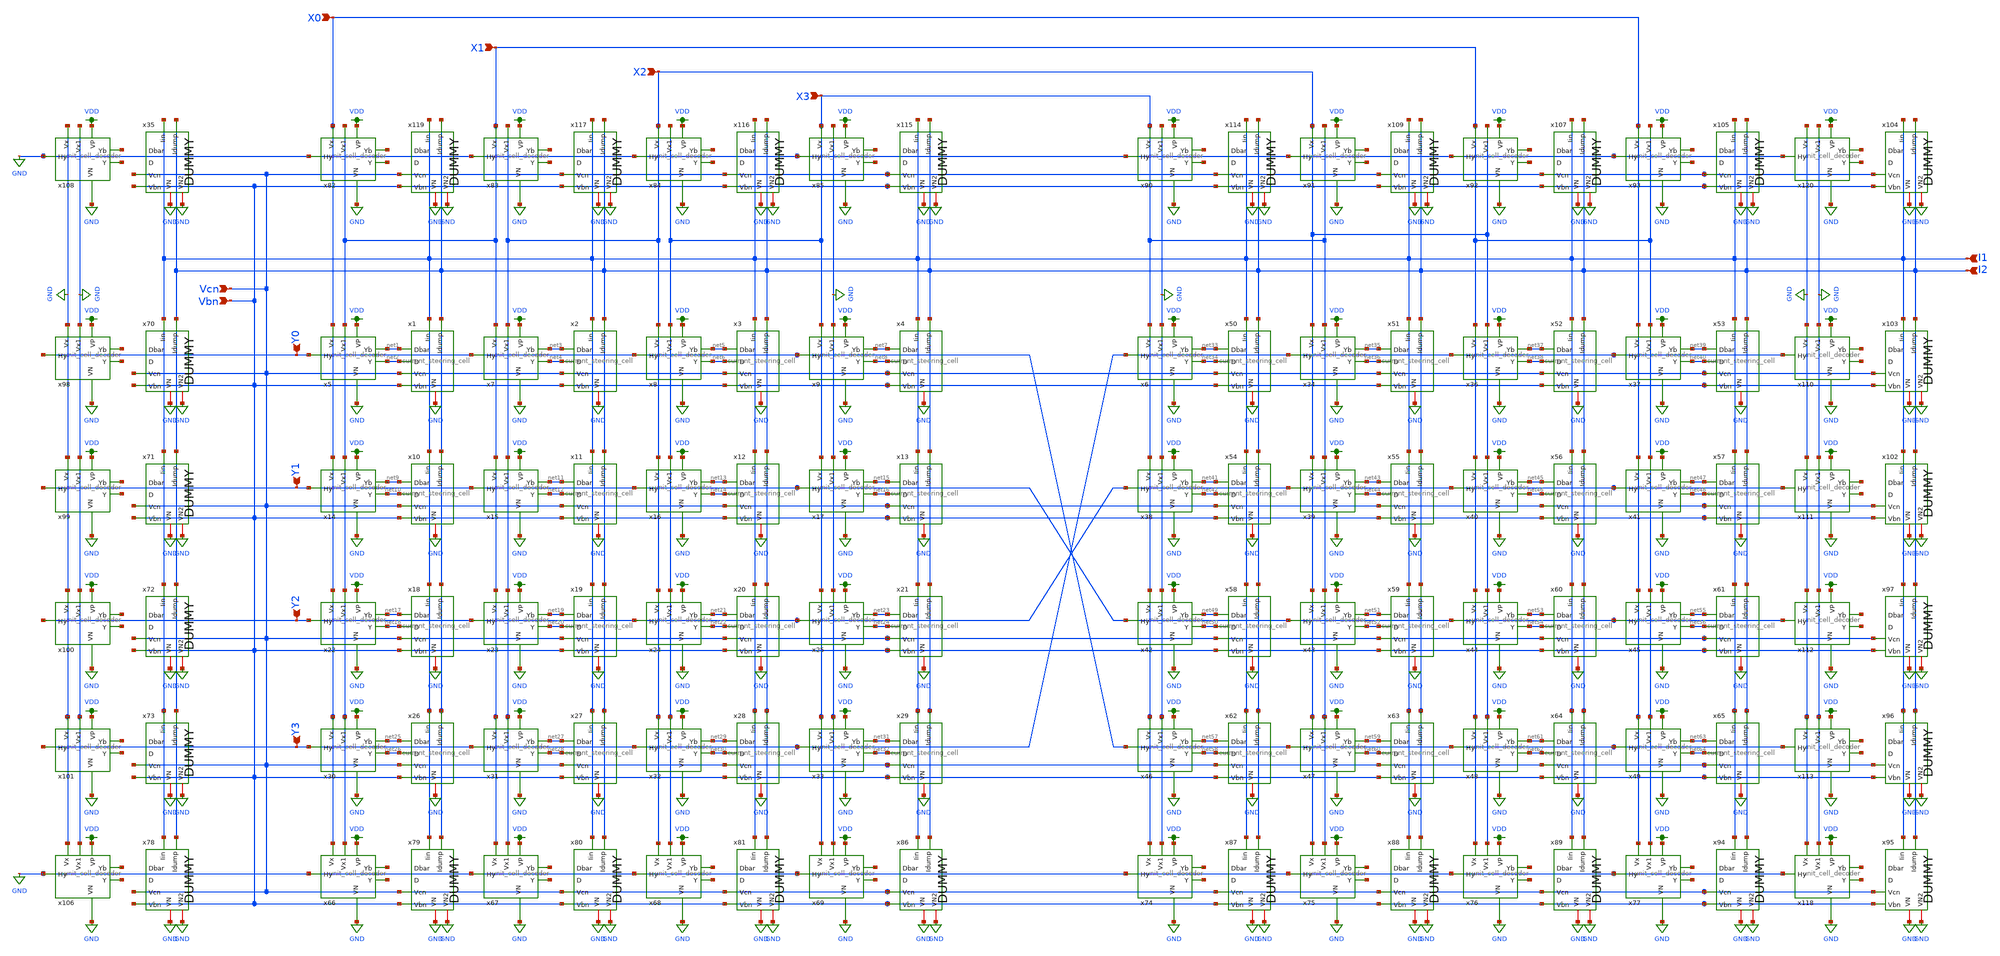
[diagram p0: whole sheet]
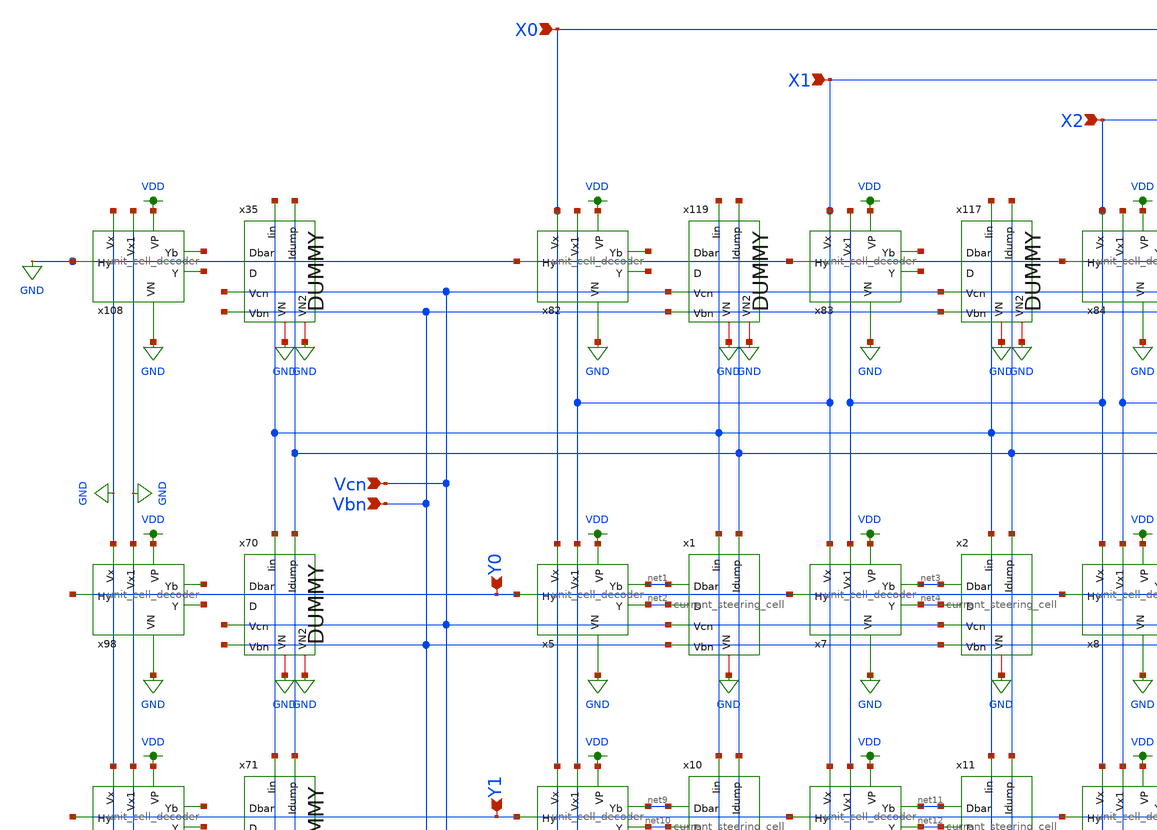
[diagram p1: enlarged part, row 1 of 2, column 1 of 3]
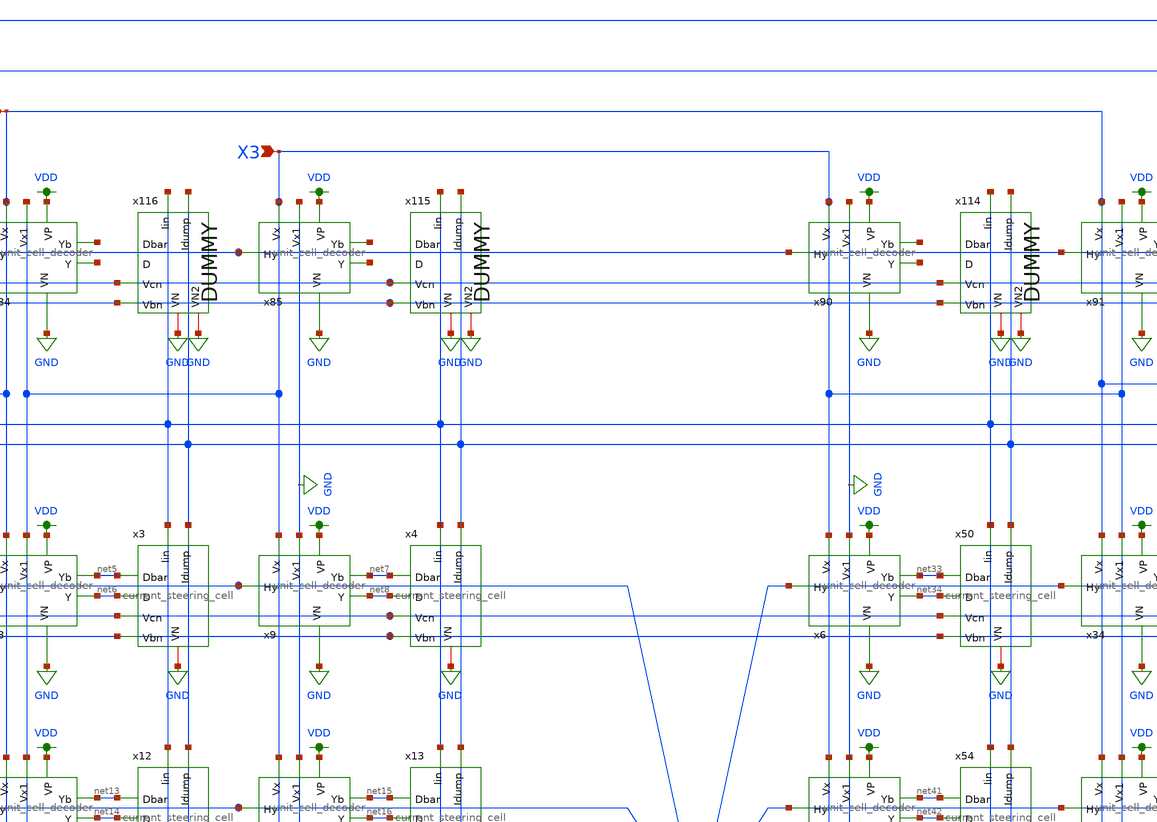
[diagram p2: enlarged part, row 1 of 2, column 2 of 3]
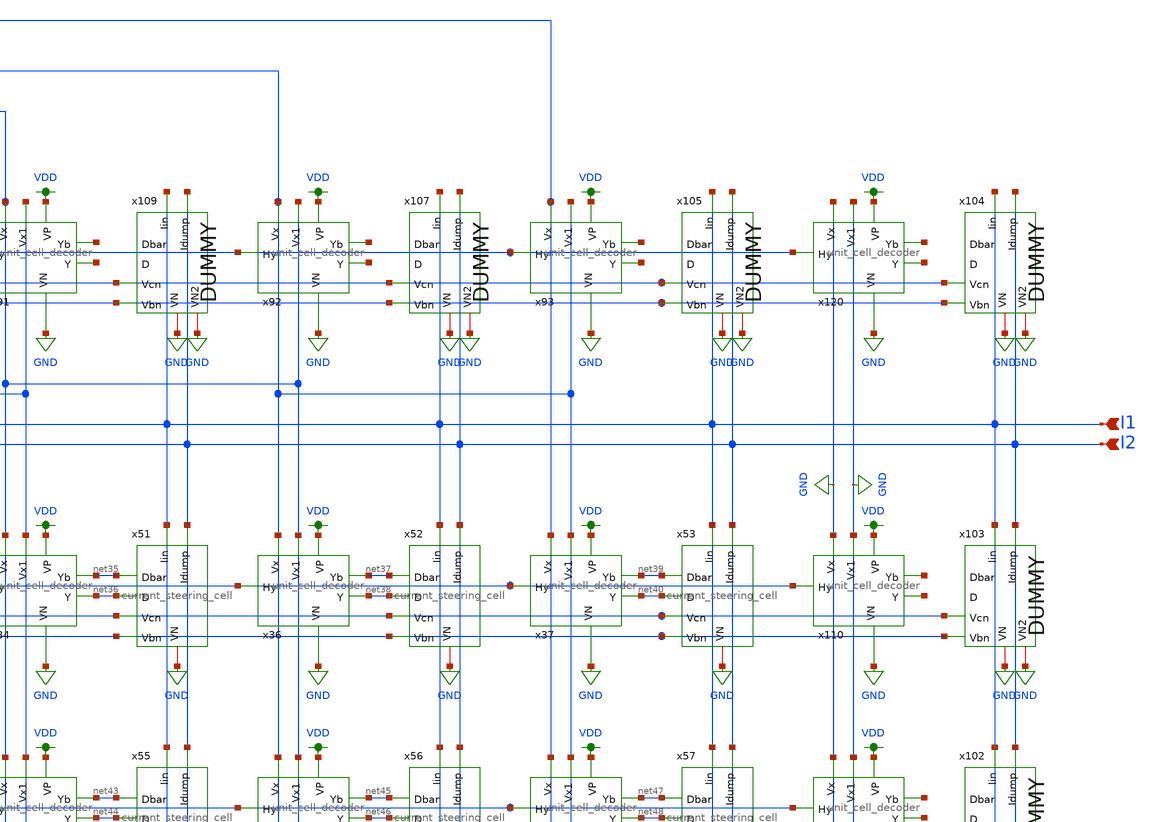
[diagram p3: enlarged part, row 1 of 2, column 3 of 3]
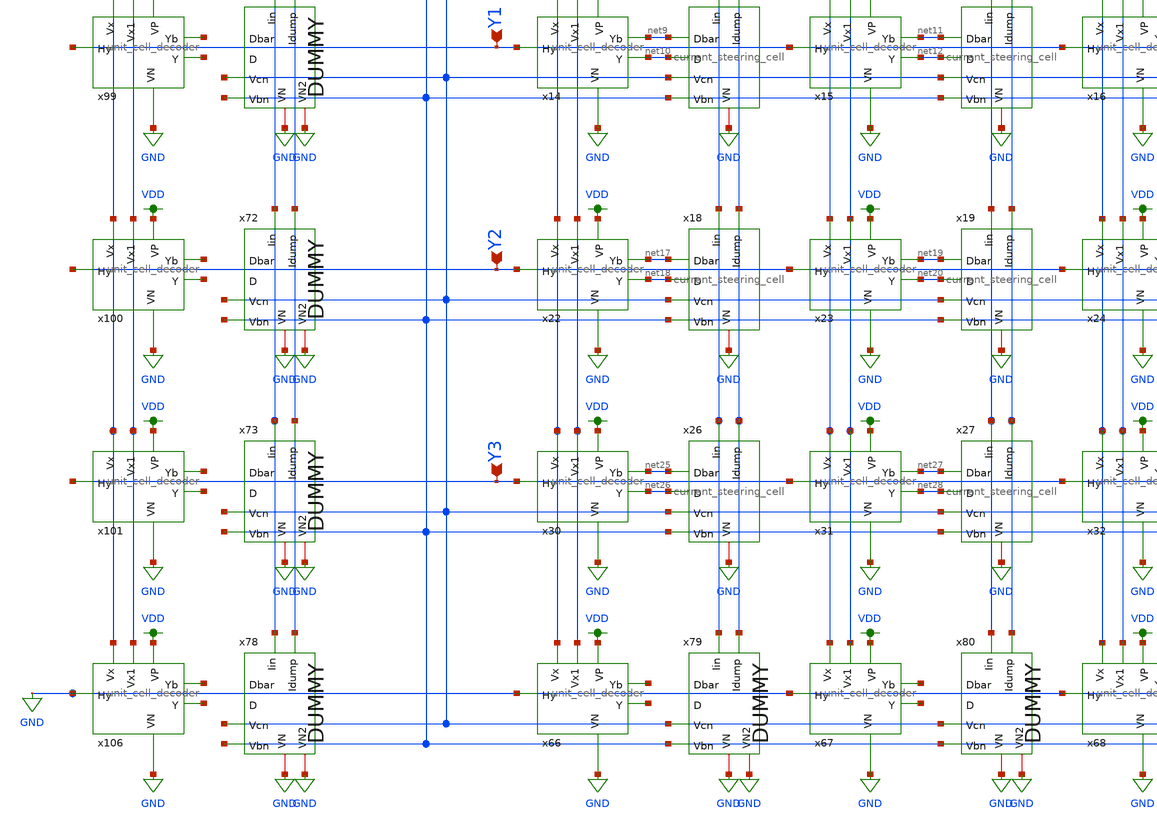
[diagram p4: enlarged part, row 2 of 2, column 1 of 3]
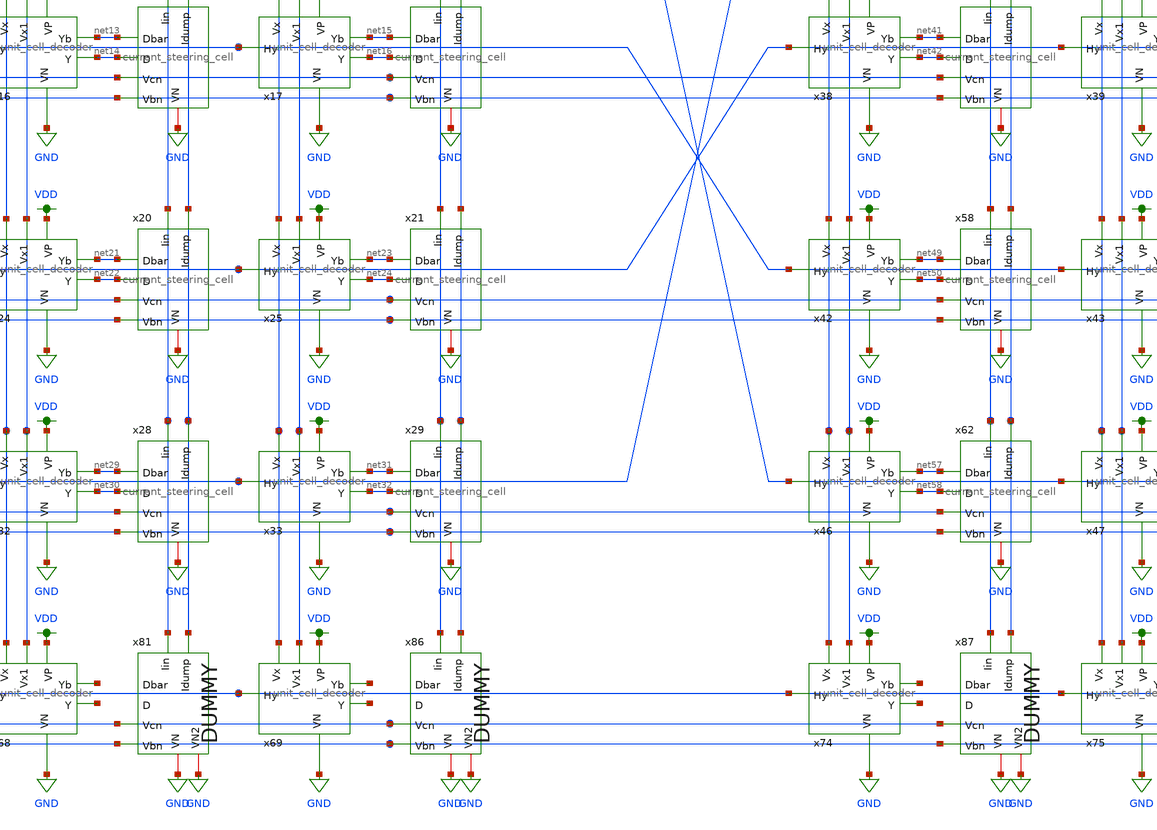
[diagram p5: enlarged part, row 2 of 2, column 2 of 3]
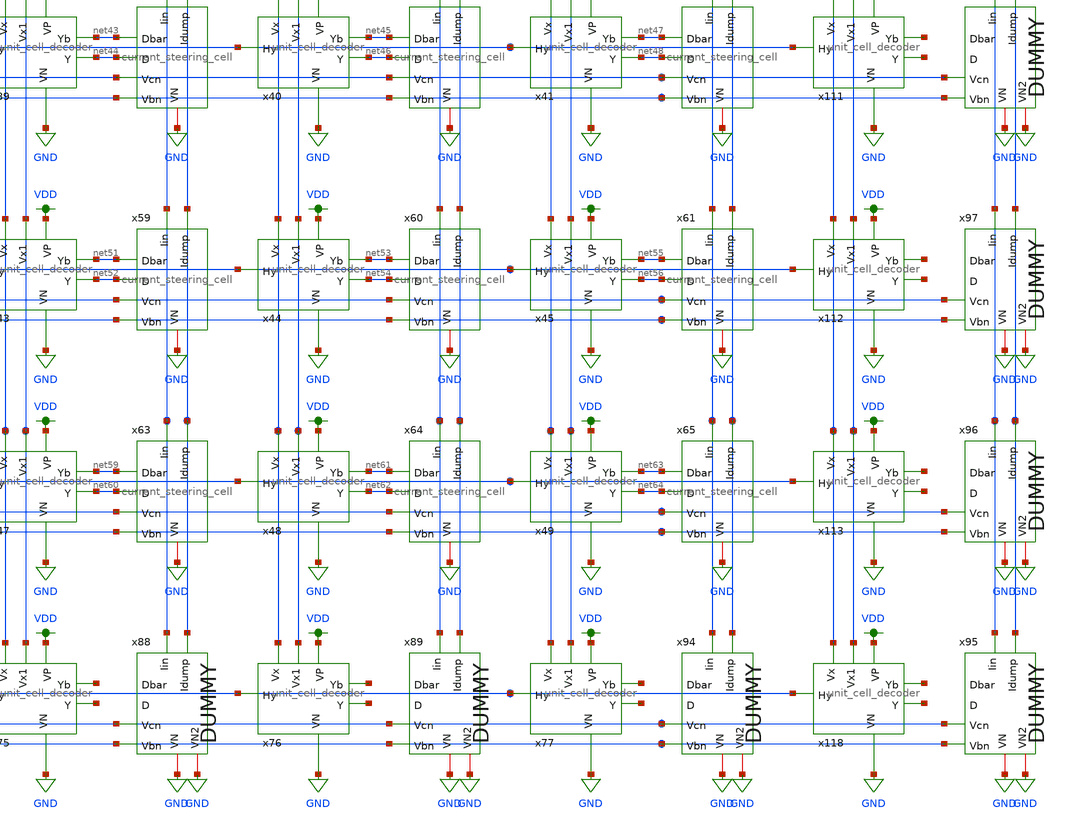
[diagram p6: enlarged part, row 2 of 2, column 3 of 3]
** sch_path: lvs/current_steering_dac.sch
**.subckt current_steering_dac I1 I2 X0 X1 X2 X3 Y0 Y1 Y2 Y3 Vcn Vbn
*.ipin I1
*.ipin I2
*.ipin X0
*.ipin X1
*.ipin X2
*.ipin X3
*.ipin Y0
*.ipin Y1
*.ipin Y2
*.ipin Y3
*.ipin Vcn
*.ipin Vbn
x5 X0 X1 Y0 VDD GND net1 net2 unit_cell_decoder
x7 X1 X2 Y0 VDD GND net3 net4 unit_cell_decoder
x8 X2 X3 Y0 VDD GND net5 net6 unit_cell_decoder
x9 X3 GND Y0 VDD GND net7 net8 unit_cell_decoder
x14 X0 X1 Y1 VDD GND net9 net10 unit_cell_decoder
x15 X1 X2 Y1 VDD GND net11 net12 unit_cell_decoder
x16 X2 X3 Y1 VDD GND net13 net14 unit_cell_decoder
x17 X3 GND Y1 VDD GND net15 net16 unit_cell_decoder
x22 X0 X1 Y2 VDD GND net17 net18 unit_cell_decoder
x23 X1 X2 Y2 VDD GND net19 net20 unit_cell_decoder
x24 X2 X3 Y2 VDD GND net21 net22 unit_cell_decoder
x25 X3 GND Y2 VDD GND net23 net24 unit_cell_decoder
x30 X0 X1 Y3 VDD GND net25 net26 unit_cell_decoder
x31 X1 X2 Y3 VDD GND net27 net28 unit_cell_decoder
x32 X2 X3 Y3 VDD GND net29 net30 unit_cell_decoder
x33 X3 GND Y3 VDD GND net31 net32 unit_cell_decoder
x1 I1 I2 net1 net2 Vcn Vbn GND current_steering_cell
x2 I1 I2 net3 net4 Vcn Vbn GND current_steering_cell
x3 I1 I2 net5 net6 Vcn Vbn GND current_steering_cell
x4 I1 I2 net7 net8 Vcn Vbn GND current_steering_cell
x10 I1 I2 net9 net10 Vcn Vbn GND current_steering_cell
x11 I1 I2 net11 net12 Vcn Vbn GND current_steering_cell
x12 I1 I2 net13 net14 Vcn Vbn GND current_steering_cell
x13 I1 I2 net15 net16 Vcn Vbn GND current_steering_cell
x18 I1 I2 net17 net18 Vcn Vbn GND current_steering_cell
x19 I1 I2 net19 net20 Vcn Vbn GND current_steering_cell
x20 I1 I2 net21 net22 Vcn Vbn GND current_steering_cell
x21 I1 I2 net23 net24 Vcn Vbn GND current_steering_cell
x26 I1 I2 net25 net26 Vcn Vbn GND current_steering_cell
x27 I1 I2 net27 net28 Vcn Vbn GND current_steering_cell
x28 I1 I2 net29 net30 Vcn Vbn GND current_steering_cell
x29 I1 I2 net31 net32 Vcn Vbn GND current_steering_cell
x6 X3 GND Y3 VDD GND net33 net34 unit_cell_decoder
x34 X2 X3 Y3 VDD GND net35 net36 unit_cell_decoder
x36 X1 X2 Y3 VDD GND net37 net38 unit_cell_decoder
x37 X0 X1 Y3 VDD GND net39 net40 unit_cell_decoder
x38 X3 GND Y2 VDD GND net41 net42 unit_cell_decoder
x39 X2 X3 Y2 VDD GND net43 net44 unit_cell_decoder
x40 X1 X2 Y2 VDD GND net45 net46 unit_cell_decoder
x41 X0 X1 Y2 VDD GND net47 net48 unit_cell_decoder
x42 X3 GND Y1 VDD GND net49 net50 unit_cell_decoder
x43 X2 X3 Y1 VDD GND net51 net52 unit_cell_decoder
x44 X1 X2 Y1 VDD GND net53 net54 unit_cell_decoder
x45 X0 X1 Y1 VDD GND net55 net56 unit_cell_decoder
x46 X3 GND Y0 VDD GND net57 net58 unit_cell_decoder
x47 X2 X3 Y0 VDD GND net59 net60 unit_cell_decoder
x48 X1 X2 Y0 VDD GND net61 net62 unit_cell_decoder
x49 X0 X1 Y0 VDD GND net63 net64 unit_cell_decoder
x50 I1 I2 net33 net34 Vcn Vbn GND current_steering_cell
x51 I1 I2 net35 net36 Vcn Vbn GND current_steering_cell
x52 I1 I2 net37 net38 Vcn Vbn GND current_steering_cell
x53 I1 I2 net39 net40 Vcn Vbn GND current_steering_cell
x54 I1 I2 net41 net42 Vcn Vbn GND current_steering_cell
x55 I1 I2 net43 net44 Vcn Vbn GND current_steering_cell
x56 I1 I2 net45 net46 Vcn Vbn GND current_steering_cell
x57 I1 I2 net47 net48 Vcn Vbn GND current_steering_cell
x58 I1 I2 net49 net50 Vcn Vbn GND current_steering_cell
x59 I1 I2 net51 net52 Vcn Vbn GND current_steering_cell
x60 I1 I2 net53 net54 Vcn Vbn GND current_steering_cell
x61 I1 I2 net55 net56 Vcn Vbn GND current_steering_cell
x62 I1 I2 net57 net58 Vcn Vbn GND current_steering_cell
x63 I1 I2 net59 net60 Vcn Vbn GND current_steering_cell
x64 I1 I2 net61 net62 Vcn Vbn GND current_steering_cell
x65 I1 I2 net63 net64 Vcn Vbn GND current_steering_cell
x66 X0 X1 GND VDD GND net65 net66 unit_cell_decoder
x67 X1 X2 GND VDD GND net67 net68 unit_cell_decoder
x68 X2 X3 GND VDD GND net69 net70 unit_cell_decoder
x69 X3 GND GND VDD GND net71 net72 unit_cell_decoder
x74 X3 GND GND VDD GND net73 net74 unit_cell_decoder
x75 X2 X3 GND VDD GND net75 net76 unit_cell_decoder
x76 X1 X2 GND VDD GND net77 net78 unit_cell_decoder
x77 X0 X1 GND VDD GND net79 net80 unit_cell_decoder
x82 X0 X1 GND VDD GND net81 net82 unit_cell_decoder
x83 X1 X2 GND VDD GND net83 net84 unit_cell_decoder
x84 X2 X3 GND VDD GND net85 net86 unit_cell_decoder
x85 X3 GND GND VDD GND net87 net88 unit_cell_decoder
x90 X3 GND GND VDD GND net89 net90 unit_cell_decoder
x91 X2 X3 GND VDD GND net91 net92 unit_cell_decoder
x92 X1 X2 GND VDD GND net93 net94 unit_cell_decoder
x93 X0 X1 GND VDD GND net95 net96 unit_cell_decoder
x98 GND GND Y0 VDD GND net97 net98 unit_cell_decoder
x99 GND GND Y1 VDD GND net99 net100 unit_cell_decoder
x100 GND GND Y2 VDD GND net101 net102 unit_cell_decoder
x101 GND GND Y3 VDD GND net103 net104 unit_cell_decoder
x106 GND GND GND VDD GND net105 net106 unit_cell_decoder
x108 GND GND GND VDD GND net107 net108 unit_cell_decoder
x110 GND GND Y3 VDD GND net109 net110 unit_cell_decoder
x111 GND GND Y2 VDD GND net111 net112 unit_cell_decoder
x112 GND GND Y1 VDD GND net113 net114 unit_cell_decoder
x113 GND GND Y0 VDD GND net115 net116 unit_cell_decoder
x118 GND GND GND VDD GND net117 net118 unit_cell_decoder
x120 GND GND GND VDD GND net119 net120 unit_cell_decoder
x35 I1 I2 Vcn Vbn GND GND dummy_current_steering_cell
x70 I1 I2 Vcn Vbn GND GND dummy_current_steering_cell
x71 I1 I2 Vcn Vbn GND GND dummy_current_steering_cell
x72 I1 I2 Vcn Vbn GND GND dummy_current_steering_cell
x73 I1 I2 Vcn Vbn GND GND dummy_current_steering_cell
x78 I1 I2 Vcn Vbn GND GND dummy_current_steering_cell
x79 I1 I2 Vcn Vbn GND GND dummy_current_steering_cell
x80 I1 I2 Vcn Vbn GND GND dummy_current_steering_cell
x81 I1 I2 Vcn Vbn GND GND dummy_current_steering_cell
x86 I1 I2 Vcn Vbn GND GND dummy_current_steering_cell
x87 I1 I2 Vcn Vbn GND GND dummy_current_steering_cell
x88 I1 I2 Vcn Vbn GND GND dummy_current_steering_cell
x89 I1 I2 Vcn Vbn GND GND dummy_current_steering_cell
x94 I1 I2 Vcn Vbn GND GND dummy_current_steering_cell
x95 I1 I2 Vcn Vbn GND GND dummy_current_steering_cell
x96 I1 I2 Vcn Vbn GND GND dummy_current_steering_cell
x97 I1 I2 Vcn Vbn GND GND dummy_current_steering_cell
x102 I1 I2 Vcn Vbn GND GND dummy_current_steering_cell
x103 I1 I2 Vcn Vbn GND GND dummy_current_steering_cell
x104 I1 I2 Vcn Vbn GND GND dummy_current_steering_cell
x105 I1 I2 Vcn Vbn GND GND dummy_current_steering_cell
x107 I1 I2 Vcn Vbn GND GND dummy_current_steering_cell
x109 I1 I2 Vcn Vbn GND GND dummy_current_steering_cell
x114 I1 I2 Vcn Vbn GND GND dummy_current_steering_cell
x115 I1 I2 Vcn Vbn GND GND dummy_current_steering_cell
x116 I1 I2 Vcn Vbn GND GND dummy_current_steering_cell
x117 I1 I2 Vcn Vbn GND GND dummy_current_steering_cell
x119 I1 I2 Vcn Vbn GND GND dummy_current_steering_cell
**.ends
.GLOBAL GND
.GLOBAL VDD
.end
